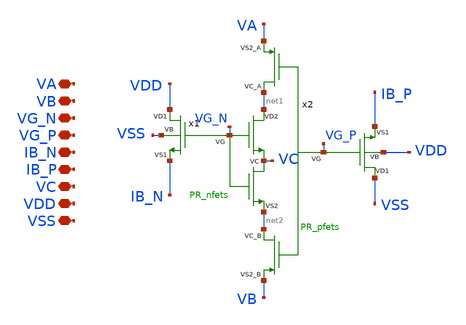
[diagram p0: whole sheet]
** sch_path: TIA_Filter/PseudoResistor/PR_net.sch
**.subckt PR_net VA VB VG_N VG_P IB_N IB_P VC VDD VSS
*.iopin VA
*.iopin VB
*.iopin VG_N
*.iopin VG_P
*.iopin IB_N
*.iopin IB_P
*.iopin VC
*.iopin VDD
*.iopin VSS
x1 VDD net1 IB_N net2 VG_N VC VSS PR_nfets
x2 VSS IB_P VA VB VG_P net1 net2 VDD PR_pfets
**.ends

* expanding   symbol:  PseudoResistor/PR_nfets.sym # of pins=7
** sym_path: TIA/xschem/PseudoResistor/PR_nfets.sym
** sch_path: TIA/xschem/PseudoResistor/PR_nfets.sch
.subckt PR_nfets VD1 VD2 VS1 VS2 VG VC VB
*.iopin VD1
*.iopin VD2
*.iopin VS1
*.iopin VS2
*.iopin VG
*.iopin VC
*.iopin VB
XM5 VB VB VB VB nfet_03v3 L=2u W=2u nf=1 ad='int((nf+1)/2) * W/nf * 0.18u' as='int((nf+2)/2) * W/nf * 0.18u'
+ pd='2*int((nf+1)/2) * (W/nf + 0.18u)' ps='2*int((nf+2)/2) * (W/nf + 0.18u)' nrd='0.18u / W' nrs='0.18u / W'
+ sa=0 sb=0 sd=0 m=32
XM3 VD2 VG net1 VB nfet_03v3 L=2u W=2u nf=1 ad='int((nf+1)/2) * W/nf * 0.18u' as='int((nf+2)/2) * W/nf * 0.18u'
+ pd='2*int((nf+1)/2) * (W/nf + 0.18u)' ps='2*int((nf+2)/2) * (W/nf + 0.18u)' nrd='0.18u / W' nrs='0.18u / W'
+ sa=0 sb=0 sd=0 m=1
XM4 net1 VG VC VB nfet_03v3 L=2u W=2u nf=1 ad='int((nf+1)/2) * W/nf * 0.18u' as='int((nf+2)/2) * W/nf * 0.18u'
+ pd='2*int((nf+1)/2) * (W/nf + 0.18u)' ps='2*int((nf+2)/2) * (W/nf + 0.18u)' nrd='0.18u / W' nrs='0.18u / W'
+ sa=0 sb=0 sd=0 m=1
XM6 VD2 VG net2 VB nfet_03v3 L=2u W=2u nf=1 ad='int((nf+1)/2) * W/nf * 0.18u' as='int((nf+2)/2) * W/nf * 0.18u'
+ pd='2*int((nf+1)/2) * (W/nf + 0.18u)' ps='2*int((nf+2)/2) * (W/nf + 0.18u)' nrd='0.18u / W' nrs='0.18u / W'
+ sa=0 sb=0 sd=0 m=1
XM8 net2 VG VC VB nfet_03v3 L=2u W=2u nf=1 ad='int((nf+1)/2) * W/nf * 0.18u' as='int((nf+2)/2) * W/nf * 0.18u'
+ pd='2*int((nf+1)/2) * (W/nf + 0.18u)' ps='2*int((nf+2)/2) * (W/nf + 0.18u)' nrd='0.18u / W' nrs='0.18u / W'
+ sa=0 sb=0 sd=0 m=1
XM1 VC VG net3 VB nfet_03v3 L=2u W=2u nf=1 ad='int((nf+1)/2) * W/nf * 0.18u' as='int((nf+2)/2) * W/nf * 0.18u'
+ pd='2*int((nf+1)/2) * (W/nf + 0.18u)' ps='2*int((nf+2)/2) * (W/nf + 0.18u)' nrd='0.18u / W' nrs='0.18u / W'
+ sa=0 sb=0 sd=0 m=1
XM9 net3 VG VS2 VB nfet_03v3 L=2u W=2u nf=1 ad='int((nf+1)/2) * W/nf * 0.18u' as='int((nf+2)/2) * W/nf * 0.18u'
+ pd='2*int((nf+1)/2) * (W/nf + 0.18u)' ps='2*int((nf+2)/2) * (W/nf + 0.18u)' nrd='0.18u / W' nrs='0.18u / W'
+ sa=0 sb=0 sd=0 m=1
XM10 VC VG net4 VB nfet_03v3 L=2u W=2u nf=1 ad='int((nf+1)/2) * W/nf * 0.18u' as='int((nf+2)/2) * W/nf * 0.18u'
+ pd='2*int((nf+1)/2) * (W/nf + 0.18u)' ps='2*int((nf+2)/2) * (W/nf + 0.18u)' nrd='0.18u / W' nrs='0.18u / W'
+ sa=0 sb=0 sd=0 m=1
XM11 net4 VG VS2 VB nfet_03v3 L=2u W=2u nf=1 ad='int((nf+1)/2) * W/nf * 0.18u' as='int((nf+2)/2) * W/nf * 0.18u'
+ pd='2*int((nf+1)/2) * (W/nf + 0.18u)' ps='2*int((nf+2)/2) * (W/nf + 0.18u)' nrd='0.18u / W' nrs='0.18u / W'
+ sa=0 sb=0 sd=0 m=1
XM2 VD1 VG net5 VB nfet_03v3 L=2u W=2u nf=1 ad='int((nf+1)/2) * W/nf * 0.18u' as='int((nf+2)/2) * W/nf * 0.18u'
+ pd='2*int((nf+1)/2) * (W/nf + 0.18u)' ps='2*int((nf+2)/2) * (W/nf + 0.18u)' nrd='0.18u / W' nrs='0.18u / W'
+ sa=0 sb=0 sd=0 m=1
XM12 net5 VG VS1 VB nfet_03v3 L=2u W=2u nf=1 ad='int((nf+1)/2) * W/nf * 0.18u' as='int((nf+2)/2) * W/nf * 0.18u'
+ pd='2*int((nf+1)/2) * (W/nf + 0.18u)' ps='2*int((nf+2)/2) * (W/nf + 0.18u)' nrd='0.18u / W' nrs='0.18u / W'
+ sa=0 sb=0 sd=0 m=1
XM13 VD1 VG net6 VB nfet_03v3 L=2u W=2u nf=1 ad='int((nf+1)/2) * W/nf * 0.18u' as='int((nf+2)/2) * W/nf * 0.18u'
+ pd='2*int((nf+1)/2) * (W/nf + 0.18u)' ps='2*int((nf+2)/2) * (W/nf + 0.18u)' nrd='0.18u / W' nrs='0.18u / W'
+ sa=0 sb=0 sd=0 m=1
XM14 net6 VG VS1 VB nfet_03v3 L=2u W=2u nf=1 ad='int((nf+1)/2) * W/nf * 0.18u' as='int((nf+2)/2) * W/nf * 0.18u'
+ pd='2*int((nf+1)/2) * (W/nf + 0.18u)' ps='2*int((nf+2)/2) * (W/nf + 0.18u)' nrd='0.18u / W' nrs='0.18u / W'
+ sa=0 sb=0 sd=0 m=1
XM7 VD1 VG net7 VB nfet_03v3 L=2u W=2u nf=1 ad='int((nf+1)/2) * W/nf * 0.18u' as='int((nf+2)/2) * W/nf * 0.18u'
+ pd='2*int((nf+1)/2) * (W/nf + 0.18u)' ps='2*int((nf+2)/2) * (W/nf + 0.18u)' nrd='0.18u / W' nrs='0.18u / W'
+ sa=0 sb=0 sd=0 m=1
XM15 net7 VG VS1 VB nfet_03v3 L=2u W=2u nf=1 ad='int((nf+1)/2) * W/nf * 0.18u' as='int((nf+2)/2) * W/nf * 0.18u'
+ pd='2*int((nf+1)/2) * (W/nf + 0.18u)' ps='2*int((nf+2)/2) * (W/nf + 0.18u)' nrd='0.18u / W' nrs='0.18u / W'
+ sa=0 sb=0 sd=0 m=1
XM16 VD1 VG net8 VB nfet_03v3 L=2u W=2u nf=1 ad='int((nf+1)/2) * W/nf * 0.18u' as='int((nf+2)/2) * W/nf * 0.18u'
+ pd='2*int((nf+1)/2) * (W/nf + 0.18u)' ps='2*int((nf+2)/2) * (W/nf + 0.18u)' nrd='0.18u / W' nrs='0.18u / W'
+ sa=0 sb=0 sd=0 m=1
XM17 net8 VG VS1 VB nfet_03v3 L=2u W=2u nf=1 ad='int((nf+1)/2) * W/nf * 0.18u' as='int((nf+2)/2) * W/nf * 0.18u'
+ pd='2*int((nf+1)/2) * (W/nf + 0.18u)' ps='2*int((nf+2)/2) * (W/nf + 0.18u)' nrd='0.18u / W' nrs='0.18u / W'
+ sa=0 sb=0 sd=0 m=1
.ends


* expanding   symbol:  PseudoResistor/PR_pfets.sym # of pins=8
** sym_path: TIA_Filter/PseudoResistor/PR_pfets.sym
** sch_path: TIA_Filter/PseudoResistor/PR_pfets.sch
.subckt PR_pfets VD1 VS1 VS2_A VS2_B VG VC_A VC_B VB
*.iopin VD1
*.iopin VS1
*.iopin VS2_A
*.iopin VS2_B
*.iopin VG
*.iopin VC_A
*.iopin VC_B
*.iopin VB
XM1 net3 VG VS1 VB pfet_03v3 L=2u W=2u nf=1 ad='int((nf+1)/2) * W/nf * 0.18u' as='int((nf+2)/2) * W/nf * 0.18u'
+ pd='2*int((nf+1)/2) * (W/nf + 0.18u)' ps='2*int((nf+2)/2) * (W/nf + 0.18u)' nrd='0.18u / W' nrs='0.18u / W'
+ sa=0 sb=0 sd=0 m=1
XM2 VD1 VG net3 VB pfet_03v3 L=2u W=2u nf=1 ad='int((nf+1)/2) * W/nf * 0.18u' as='int((nf+2)/2) * W/nf * 0.18u'
+ pd='2*int((nf+1)/2) * (W/nf + 0.18u)' ps='2*int((nf+2)/2) * (W/nf + 0.18u)' nrd='0.18u / W' nrs='0.18u / W'
+ sa=0 sb=0 sd=0 m=1
XM5 net4 VG VS1 VB pfet_03v3 L=2u W=2u nf=1 ad='int((nf+1)/2) * W/nf * 0.18u' as='int((nf+2)/2) * W/nf * 0.18u'
+ pd='2*int((nf+1)/2) * (W/nf + 0.18u)' ps='2*int((nf+2)/2) * (W/nf + 0.18u)' nrd='0.18u / W' nrs='0.18u / W'
+ sa=0 sb=0 sd=0 m=1
XM6 VD1 VG net4 VB pfet_03v3 L=2u W=2u nf=1 ad='int((nf+1)/2) * W/nf * 0.18u' as='int((nf+2)/2) * W/nf * 0.18u'
+ pd='2*int((nf+1)/2) * (W/nf + 0.18u)' ps='2*int((nf+2)/2) * (W/nf + 0.18u)' nrd='0.18u / W' nrs='0.18u / W'
+ sa=0 sb=0 sd=0 m=1
XM7 net5 VG VS1 VB pfet_03v3 L=2u W=2u nf=1 ad='int((nf+1)/2) * W/nf * 0.18u' as='int((nf+2)/2) * W/nf * 0.18u'
+ pd='2*int((nf+1)/2) * (W/nf + 0.18u)' ps='2*int((nf+2)/2) * (W/nf + 0.18u)' nrd='0.18u / W' nrs='0.18u / W'
+ sa=0 sb=0 sd=0 m=1
XM9 VD1 VG net5 VB pfet_03v3 L=2u W=2u nf=1 ad='int((nf+1)/2) * W/nf * 0.18u' as='int((nf+2)/2) * W/nf * 0.18u'
+ pd='2*int((nf+1)/2) * (W/nf + 0.18u)' ps='2*int((nf+2)/2) * (W/nf + 0.18u)' nrd='0.18u / W' nrs='0.18u / W'
+ sa=0 sb=0 sd=0 m=1
XM10 net6 VG VS1 VB pfet_03v3 L=2u W=2u nf=1 ad='int((nf+1)/2) * W/nf * 0.18u' as='int((nf+2)/2) * W/nf * 0.18u'
+ pd='2*int((nf+1)/2) * (W/nf + 0.18u)' ps='2*int((nf+2)/2) * (W/nf + 0.18u)' nrd='0.18u / W' nrs='0.18u / W'
+ sa=0 sb=0 sd=0 m=1
XM11 VD1 VG net6 VB pfet_03v3 L=2u W=2u nf=1 ad='int((nf+1)/2) * W/nf * 0.18u' as='int((nf+2)/2) * W/nf * 0.18u'
+ pd='2*int((nf+1)/2) * (W/nf + 0.18u)' ps='2*int((nf+2)/2) * (W/nf + 0.18u)' nrd='0.18u / W' nrs='0.18u / W'
+ sa=0 sb=0 sd=0 m=1
XM12 net1 VG VS2_A VBpr pfet_03v3 L=2u W=2u nf=1 ad='int((nf+1)/2) * W/nf * 0.18u' as='int((nf+2)/2) * W/nf * 0.18u'
+ pd='2*int((nf+1)/2) * (W/nf + 0.18u)' ps='2*int((nf+2)/2) * (W/nf + 0.18u)' nrd='0.18u / W' nrs='0.18u / W'
+ sa=0 sb=0 sd=0 m=1
XM13 VC_A VG net1 VBpr pfet_03v3 L=2u W=2u nf=1 ad='int((nf+1)/2) * W/nf * 0.18u' as='int((nf+2)/2) * W/nf * 0.18u'
+ pd='2*int((nf+1)/2) * (W/nf + 0.18u)' ps='2*int((nf+2)/2) * (W/nf + 0.18u)' nrd='0.18u / W' nrs='0.18u / W'
+ sa=0 sb=0 sd=0 m=1
XM14 net2 VG VS2_A VBpr pfet_03v3 L=2u W=2u nf=1 ad='int((nf+1)/2) * W/nf * 0.18u' as='int((nf+2)/2) * W/nf * 0.18u'
+ pd='2*int((nf+1)/2) * (W/nf + 0.18u)' ps='2*int((nf+2)/2) * (W/nf + 0.18u)' nrd='0.18u / W' nrs='0.18u / W'
+ sa=0 sb=0 sd=0 m=1
XM15 VC_A VG net2 VBpr pfet_03v3 L=2u W=2u nf=1 ad='int((nf+1)/2) * W/nf * 0.18u' as='int((nf+2)/2) * W/nf * 0.18u'
+ pd='2*int((nf+1)/2) * (W/nf + 0.18u)' ps='2*int((nf+2)/2) * (W/nf + 0.18u)' nrd='0.18u / W' nrs='0.18u / W'
+ sa=0 sb=0 sd=0 m=1
XM16 VC_B VG net7 VBpr pfet_03v3 L=2u W=2u nf=1 ad='int((nf+1)/2) * W/nf * 0.18u' as='int((nf+2)/2) * W/nf * 0.18u'
+ pd='2*int((nf+1)/2) * (W/nf + 0.18u)' ps='2*int((nf+2)/2) * (W/nf + 0.18u)' nrd='0.18u / W' nrs='0.18u / W'
+ sa=0 sb=0 sd=0 m=1
XM17 net7 VG VS2_B VBpr pfet_03v3 L=2u W=2u nf=1 ad='int((nf+1)/2) * W/nf * 0.18u' as='int((nf+2)/2) * W/nf * 0.18u'
+ pd='2*int((nf+1)/2) * (W/nf + 0.18u)' ps='2*int((nf+2)/2) * (W/nf + 0.18u)' nrd='0.18u / W' nrs='0.18u / W'
+ sa=0 sb=0 sd=0 m=1
XM18 VC_B VG net8 VBpr pfet_03v3 L=2u W=2u nf=1 ad='int((nf+1)/2) * W/nf * 0.18u' as='int((nf+2)/2) * W/nf * 0.18u'
+ pd='2*int((nf+1)/2) * (W/nf + 0.18u)' ps='2*int((nf+2)/2) * (W/nf + 0.18u)' nrd='0.18u / W' nrs='0.18u / W'
+ sa=0 sb=0 sd=0 m=1
XM19 net8 VG VS2_B VBpr pfet_03v3 L=2u W=2u nf=1 ad='int((nf+1)/2) * W/nf * 0.18u' as='int((nf+2)/2) * W/nf * 0.18u'
+ pd='2*int((nf+1)/2) * (W/nf + 0.18u)' ps='2*int((nf+2)/2) * (W/nf + 0.18u)' nrd='0.18u / W' nrs='0.18u / W'
+ sa=0 sb=0 sd=0 m=1
XM3[1] VB VB VB VB pfet_03v3 L=2u W=2u nf=1 ad='int((nf+1)/2) * W/nf * 0.18u' as='int((nf+2)/2) * W/nf * 0.18u'
+ pd='2*int((nf+1)/2) * (W/nf + 0.18u)' ps='2*int((nf+2)/2) * (W/nf + 0.18u)' nrd='0.18u / W' nrs='0.18u / W'
+ sa=0 sb=0 sd=0 m=1
XM3[2] VB VB VB VB pfet_03v3 L=2u W=2u nf=1 ad='int((nf+1)/2) * W/nf * 0.18u' as='int((nf+2)/2) * W/nf * 0.18u'
+ pd='2*int((nf+1)/2) * (W/nf + 0.18u)' ps='2*int((nf+2)/2) * (W/nf + 0.18u)' nrd='0.18u / W' nrs='0.18u / W'
+ sa=0 sb=0 sd=0 m=1
XM3[3] VB VB VB VB pfet_03v3 L=2u W=2u nf=1 ad='int((nf+1)/2) * W/nf * 0.18u' as='int((nf+2)/2) * W/nf * 0.18u'
+ pd='2*int((nf+1)/2) * (W/nf + 0.18u)' ps='2*int((nf+2)/2) * (W/nf + 0.18u)' nrd='0.18u / W' nrs='0.18u / W'
+ sa=0 sb=0 sd=0 m=1
XM3[4] VB VB VB VB pfet_03v3 L=2u W=2u nf=1 ad='int((nf+1)/2) * W/nf * 0.18u' as='int((nf+2)/2) * W/nf * 0.18u'
+ pd='2*int((nf+1)/2) * (W/nf + 0.18u)' ps='2*int((nf+2)/2) * (W/nf + 0.18u)' nrd='0.18u / W' nrs='0.18u / W'
+ sa=0 sb=0 sd=0 m=1
XM3[5] VB VB VB VB pfet_03v3 L=2u W=2u nf=1 ad='int((nf+1)/2) * W/nf * 0.18u' as='int((nf+2)/2) * W/nf * 0.18u'
+ pd='2*int((nf+1)/2) * (W/nf + 0.18u)' ps='2*int((nf+2)/2) * (W/nf + 0.18u)' nrd='0.18u / W' nrs='0.18u / W'
+ sa=0 sb=0 sd=0 m=1
XM3[6] VB VB VB VB pfet_03v3 L=2u W=2u nf=1 ad='int((nf+1)/2) * W/nf * 0.18u' as='int((nf+2)/2) * W/nf * 0.18u'
+ pd='2*int((nf+1)/2) * (W/nf + 0.18u)' ps='2*int((nf+2)/2) * (W/nf + 0.18u)' nrd='0.18u / W' nrs='0.18u / W'
+ sa=0 sb=0 sd=0 m=1
XM3[7] VB VB VB VB pfet_03v3 L=2u W=2u nf=1 ad='int((nf+1)/2) * W/nf * 0.18u' as='int((nf+2)/2) * W/nf * 0.18u'
+ pd='2*int((nf+1)/2) * (W/nf + 0.18u)' ps='2*int((nf+2)/2) * (W/nf + 0.18u)' nrd='0.18u / W' nrs='0.18u / W'
+ sa=0 sb=0 sd=0 m=1
XM3[8] VB VB VB VB pfet_03v3 L=2u W=2u nf=1 ad='int((nf+1)/2) * W/nf * 0.18u' as='int((nf+2)/2) * W/nf * 0.18u'
+ pd='2*int((nf+1)/2) * (W/nf + 0.18u)' ps='2*int((nf+2)/2) * (W/nf + 0.18u)' nrd='0.18u / W' nrs='0.18u / W'
+ sa=0 sb=0 sd=0 m=1
XM3[9] VB VB VB VB pfet_03v3 L=2u W=2u nf=1 ad='int((nf+1)/2) * W/nf * 0.18u' as='int((nf+2)/2) * W/nf * 0.18u'
+ pd='2*int((nf+1)/2) * (W/nf + 0.18u)' ps='2*int((nf+2)/2) * (W/nf + 0.18u)' nrd='0.18u / W' nrs='0.18u / W'
+ sa=0 sb=0 sd=0 m=1
XM3[10] VB VB VB VB pfet_03v3 L=2u W=2u nf=1 ad='int((nf+1)/2) * W/nf * 0.18u' as='int((nf+2)/2) * W/nf * 0.18u'
+ pd='2*int((nf+1)/2) * (W/nf + 0.18u)' ps='2*int((nf+2)/2) * (W/nf + 0.18u)' nrd='0.18u / W' nrs='0.18u / W'
+ sa=0 sb=0 sd=0 m=1
XM3[11] VB VB VB VB pfet_03v3 L=2u W=2u nf=1 ad='int((nf+1)/2) * W/nf * 0.18u' as='int((nf+2)/2) * W/nf * 0.18u'
+ pd='2*int((nf+1)/2) * (W/nf + 0.18u)' ps='2*int((nf+2)/2) * (W/nf + 0.18u)' nrd='0.18u / W' nrs='0.18u / W'
+ sa=0 sb=0 sd=0 m=1
XM3[12] VB VB VB VB pfet_03v3 L=2u W=2u nf=1 ad='int((nf+1)/2) * W/nf * 0.18u' as='int((nf+2)/2) * W/nf * 0.18u'
+ pd='2*int((nf+1)/2) * (W/nf + 0.18u)' ps='2*int((nf+2)/2) * (W/nf + 0.18u)' nrd='0.18u / W' nrs='0.18u / W'
+ sa=0 sb=0 sd=0 m=1
XM3[13] VB VB VB VB pfet_03v3 L=2u W=2u nf=1 ad='int((nf+1)/2) * W/nf * 0.18u' as='int((nf+2)/2) * W/nf * 0.18u'
+ pd='2*int((nf+1)/2) * (W/nf + 0.18u)' ps='2*int((nf+2)/2) * (W/nf + 0.18u)' nrd='0.18u / W' nrs='0.18u / W'
+ sa=0 sb=0 sd=0 m=1
XM3[14] VB VB VB VB pfet_03v3 L=2u W=2u nf=1 ad='int((nf+1)/2) * W/nf * 0.18u' as='int((nf+2)/2) * W/nf * 0.18u'
+ pd='2*int((nf+1)/2) * (W/nf + 0.18u)' ps='2*int((nf+2)/2) * (W/nf + 0.18u)' nrd='0.18u / W' nrs='0.18u / W'
+ sa=0 sb=0 sd=0 m=1
XM3[15] VB VB VB VB pfet_03v3 L=2u W=2u nf=1 ad='int((nf+1)/2) * W/nf * 0.18u' as='int((nf+2)/2) * W/nf * 0.18u'
+ pd='2*int((nf+1)/2) * (W/nf + 0.18u)' ps='2*int((nf+2)/2) * (W/nf + 0.18u)' nrd='0.18u / W' nrs='0.18u / W'
+ sa=0 sb=0 sd=0 m=1
XM3[16] VB VB VB VB pfet_03v3 L=2u W=2u nf=1 ad='int((nf+1)/2) * W/nf * 0.18u' as='int((nf+2)/2) * W/nf * 0.18u'
+ pd='2*int((nf+1)/2) * (W/nf + 0.18u)' ps='2*int((nf+2)/2) * (W/nf + 0.18u)' nrd='0.18u / W' nrs='0.18u / W'
+ sa=0 sb=0 sd=0 m=1
XM3[17] VB VB VB VB pfet_03v3 L=2u W=2u nf=1 ad='int((nf+1)/2) * W/nf * 0.18u' as='int((nf+2)/2) * W/nf * 0.18u'
+ pd='2*int((nf+1)/2) * (W/nf + 0.18u)' ps='2*int((nf+2)/2) * (W/nf + 0.18u)' nrd='0.18u / W' nrs='0.18u / W'
+ sa=0 sb=0 sd=0 m=1
XM3[18] VB VB VB VB pfet_03v3 L=2u W=2u nf=1 ad='int((nf+1)/2) * W/nf * 0.18u' as='int((nf+2)/2) * W/nf * 0.18u'
+ pd='2*int((nf+1)/2) * (W/nf + 0.18u)' ps='2*int((nf+2)/2) * (W/nf + 0.18u)' nrd='0.18u / W' nrs='0.18u / W'
+ sa=0 sb=0 sd=0 m=1
XM3[19] VB VB VB VB pfet_03v3 L=2u W=2u nf=1 ad='int((nf+1)/2) * W/nf * 0.18u' as='int((nf+2)/2) * W/nf * 0.18u'
+ pd='2*int((nf+1)/2) * (W/nf + 0.18u)' ps='2*int((nf+2)/2) * (W/nf + 0.18u)' nrd='0.18u / W' nrs='0.18u / W'
+ sa=0 sb=0 sd=0 m=1
XM3[20] VB VB VB VB pfet_03v3 L=2u W=2u nf=1 ad='int((nf+1)/2) * W/nf * 0.18u' as='int((nf+2)/2) * W/nf * 0.18u'
+ pd='2*int((nf+1)/2) * (W/nf + 0.18u)' ps='2*int((nf+2)/2) * (W/nf + 0.18u)' nrd='0.18u / W' nrs='0.18u / W'
+ sa=0 sb=0 sd=0 m=1
XM3[21] VB VB VB VB pfet_03v3 L=2u W=2u nf=1 ad='int((nf+1)/2) * W/nf * 0.18u' as='int((nf+2)/2) * W/nf * 0.18u'
+ pd='2*int((nf+1)/2) * (W/nf + 0.18u)' ps='2*int((nf+2)/2) * (W/nf + 0.18u)' nrd='0.18u / W' nrs='0.18u / W'
+ sa=0 sb=0 sd=0 m=1
XM3[22] VB VB VB VB pfet_03v3 L=2u W=2u nf=1 ad='int((nf+1)/2) * W/nf * 0.18u' as='int((nf+2)/2) * W/nf * 0.18u'
+ pd='2*int((nf+1)/2) * (W/nf + 0.18u)' ps='2*int((nf+2)/2) * (W/nf + 0.18u)' nrd='0.18u / W' nrs='0.18u / W'
+ sa=0 sb=0 sd=0 m=1
XM3[23] VB VB VB VB pfet_03v3 L=2u W=2u nf=1 ad='int((nf+1)/2) * W/nf * 0.18u' as='int((nf+2)/2) * W/nf * 0.18u'
+ pd='2*int((nf+1)/2) * (W/nf + 0.18u)' ps='2*int((nf+2)/2) * (W/nf + 0.18u)' nrd='0.18u / W' nrs='0.18u / W'
+ sa=0 sb=0 sd=0 m=1
XM3[24] VB VB VB VB pfet_03v3 L=2u W=2u nf=1 ad='int((nf+1)/2) * W/nf * 0.18u' as='int((nf+2)/2) * W/nf * 0.18u'
+ pd='2*int((nf+1)/2) * (W/nf + 0.18u)' ps='2*int((nf+2)/2) * (W/nf + 0.18u)' nrd='0.18u / W' nrs='0.18u / W'
+ sa=0 sb=0 sd=0 m=1
XM3[25] VB VB VB VB pfet_03v3 L=2u W=2u nf=1 ad='int((nf+1)/2) * W/nf * 0.18u' as='int((nf+2)/2) * W/nf * 0.18u'
+ pd='2*int((nf+1)/2) * (W/nf + 0.18u)' ps='2*int((nf+2)/2) * (W/nf + 0.18u)' nrd='0.18u / W' nrs='0.18u / W'
+ sa=0 sb=0 sd=0 m=1
XM3[26] VB VB VB VB pfet_03v3 L=2u W=2u nf=1 ad='int((nf+1)/2) * W/nf * 0.18u' as='int((nf+2)/2) * W/nf * 0.18u'
+ pd='2*int((nf+1)/2) * (W/nf + 0.18u)' ps='2*int((nf+2)/2) * (W/nf + 0.18u)' nrd='0.18u / W' nrs='0.18u / W'
+ sa=0 sb=0 sd=0 m=1
XM3[27] VB VB VB VB pfet_03v3 L=2u W=2u nf=1 ad='int((nf+1)/2) * W/nf * 0.18u' as='int((nf+2)/2) * W/nf * 0.18u'
+ pd='2*int((nf+1)/2) * (W/nf + 0.18u)' ps='2*int((nf+2)/2) * (W/nf + 0.18u)' nrd='0.18u / W' nrs='0.18u / W'
+ sa=0 sb=0 sd=0 m=1
XM3[28] VB VB VB VB pfet_03v3 L=2u W=2u nf=1 ad='int((nf+1)/2) * W/nf * 0.18u' as='int((nf+2)/2) * W/nf * 0.18u'
+ pd='2*int((nf+1)/2) * (W/nf + 0.18u)' ps='2*int((nf+2)/2) * (W/nf + 0.18u)' nrd='0.18u / W' nrs='0.18u / W'
+ sa=0 sb=0 sd=0 m=1
XM3[29] VB VB VB VB pfet_03v3 L=2u W=2u nf=1 ad='int((nf+1)/2) * W/nf * 0.18u' as='int((nf+2)/2) * W/nf * 0.18u'
+ pd='2*int((nf+1)/2) * (W/nf + 0.18u)' ps='2*int((nf+2)/2) * (W/nf + 0.18u)' nrd='0.18u / W' nrs='0.18u / W'
+ sa=0 sb=0 sd=0 m=1
XM3[30] VB VB VB VB pfet_03v3 L=2u W=2u nf=1 ad='int((nf+1)/2) * W/nf * 0.18u' as='int((nf+2)/2) * W/nf * 0.18u'
+ pd='2*int((nf+1)/2) * (W/nf + 0.18u)' ps='2*int((nf+2)/2) * (W/nf + 0.18u)' nrd='0.18u / W' nrs='0.18u / W'
+ sa=0 sb=0 sd=0 m=1
XM3[31] VB VB VB VB pfet_03v3 L=2u W=2u nf=1 ad='int((nf+1)/2) * W/nf * 0.18u' as='int((nf+2)/2) * W/nf * 0.18u'
+ pd='2*int((nf+1)/2) * (W/nf + 0.18u)' ps='2*int((nf+2)/2) * (W/nf + 0.18u)' nrd='0.18u / W' nrs='0.18u / W'
+ sa=0 sb=0 sd=0 m=1
XM3[32] VB VB VB VB pfet_03v3 L=2u W=2u nf=1 ad='int((nf+1)/2) * W/nf * 0.18u' as='int((nf+2)/2) * W/nf * 0.18u'
+ pd='2*int((nf+1)/2) * (W/nf + 0.18u)' ps='2*int((nf+2)/2) * (W/nf + 0.18u)' nrd='0.18u / W' nrs='0.18u / W'
+ sa=0 sb=0 sd=0 m=1
V_leak_P VB VBpr 0
.save i(v_leak_p)
.ends

.end
